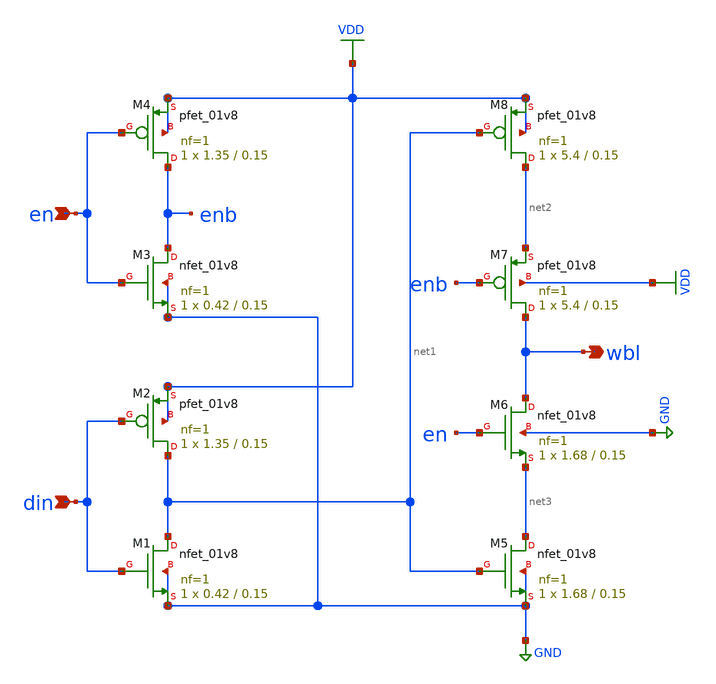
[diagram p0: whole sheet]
** sch_path: xschem/write_driver_multiport.sch
**.subckt write_driver_multiport en din wbl
*.ipin en
*.ipin din
*.opin wbl
XM1 net1 din GND GND sky130_fd_pr__nfet_01v8 L=0.15 W=0.42 nf=1 ad='int((nf+1)/2) * W/nf * 0.29' as='int((nf+2)/2) * W/nf * 0.29'
+ pd='2*int((nf+1)/2) * (W/nf + 0.29)' ps='2*int((nf+2)/2) * (W/nf + 0.29)' nrd='0.29 / W' nrs='0.29 / W'
+ sa=0 sb=0 sd=0 mult=1 m=1
XM2 net1 din VDD VDD sky130_fd_pr__pfet_01v8 L=0.15 W=1.35 nf=1 ad='int((nf+1)/2) * W/nf * 0.29' as='int((nf+2)/2) * W/nf * 0.29'
+ pd='2*int((nf+1)/2) * (W/nf + 0.29)' ps='2*int((nf+2)/2) * (W/nf + 0.29)' nrd='0.29 / W' nrs='0.29 / W'
+ sa=0 sb=0 sd=0 mult=1 m=1
XM3 enb en GND GND sky130_fd_pr__nfet_01v8 L=0.15 W=0.42 nf=1 ad='int((nf+1)/2) * W/nf * 0.29' as='int((nf+2)/2) * W/nf * 0.29'
+ pd='2*int((nf+1)/2) * (W/nf + 0.29)' ps='2*int((nf+2)/2) * (W/nf + 0.29)' nrd='0.29 / W' nrs='0.29 / W'
+ sa=0 sb=0 sd=0 mult=1 m=1
XM4 enb en VDD VDD sky130_fd_pr__pfet_01v8 L=0.15 W=1.35 nf=1 ad='int((nf+1)/2) * W/nf * 0.29' as='int((nf+2)/2) * W/nf * 0.29'
+ pd='2*int((nf+1)/2) * (W/nf + 0.29)' ps='2*int((nf+2)/2) * (W/nf + 0.29)' nrd='0.29 / W' nrs='0.29 / W'
+ sa=0 sb=0 sd=0 mult=1 m=1
XM5 net3 net1 GND GND sky130_fd_pr__nfet_01v8 L=0.15 W=1.68 nf=1 ad='int((nf+1)/2) * W/nf * 0.29' as='int((nf+2)/2) * W/nf * 0.29'
+ pd='2*int((nf+1)/2) * (W/nf + 0.29)' ps='2*int((nf+2)/2) * (W/nf + 0.29)' nrd='0.29 / W' nrs='0.29 / W'
+ sa=0 sb=0 sd=0 mult=1 m=1
XM6 wbl en net3 GND sky130_fd_pr__nfet_01v8 L=0.15 W=1.68 nf=1 ad='int((nf+1)/2) * W/nf * 0.29' as='int((nf+2)/2) * W/nf * 0.29'
+ pd='2*int((nf+1)/2) * (W/nf + 0.29)' ps='2*int((nf+2)/2) * (W/nf + 0.29)' nrd='0.29 / W' nrs='0.29 / W'
+ sa=0 sb=0 sd=0 mult=1 m=1
XM7 wbl enb net2 VDD sky130_fd_pr__pfet_01v8 L=0.15 W=5.4 nf=1 ad='int((nf+1)/2) * W/nf * 0.29' as='int((nf+2)/2) * W/nf * 0.29'
+ pd='2*int((nf+1)/2) * (W/nf + 0.29)' ps='2*int((nf+2)/2) * (W/nf + 0.29)' nrd='0.29 / W' nrs='0.29 / W'
+ sa=0 sb=0 sd=0 mult=1 m=1
XM8 net2 net1 VDD VDD sky130_fd_pr__pfet_01v8 L=0.15 W=5.4 nf=1 ad='int((nf+1)/2) * W/nf * 0.29' as='int((nf+2)/2) * W/nf * 0.29'
+ pd='2*int((nf+1)/2) * (W/nf + 0.29)' ps='2*int((nf+2)/2) * (W/nf + 0.29)' nrd='0.29 / W' nrs='0.29 / W'
+ sa=0 sb=0 sd=0 mult=1 m=1
**.ends
.GLOBAL VDD
.GLOBAL GND
.end
